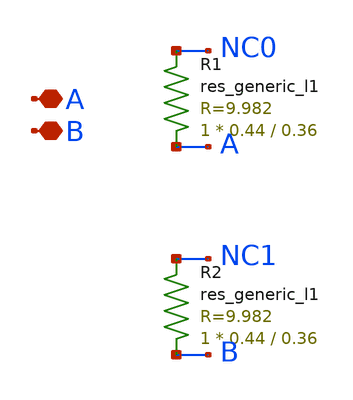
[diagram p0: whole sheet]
** sch_path: ip/sun_tr_sky130nm/design/SUN_TR_SKY130NM/SUNTR_DCAPX1_CV.sch
**.subckt SUNTR_DCAPX1_CV A B
*.iopin A
*.iopin B
R1 A NC0 sky130_fd_pr__res_generic_l1 W=0.44 L=0.36 m=1
R2 B NC1 sky130_fd_pr__res_generic_l1 W=0.44 L=0.36 m=1
**.ends
.end
